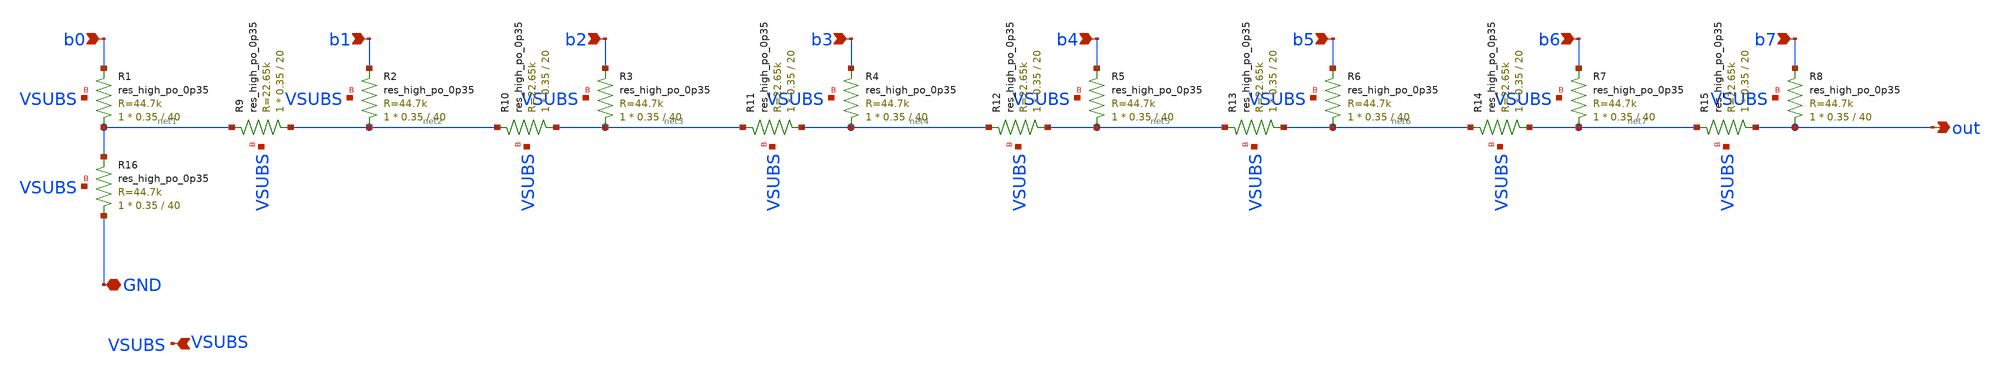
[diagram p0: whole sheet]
** sch_path: xschem/r2r.sch
**.subckt r2r b0 b1 b2 b3 b4 b5 b6 b7 out VSUBS GND
*.ipin b0
*.ipin b1
*.ipin b2
*.ipin b3
*.ipin b4
*.ipin b5
*.ipin b6
*.ipin b7
*.opin out
*.ipin VSUBS
*.iopin GND
XR1 net1 b0 VSUBS sky130_fd_pr__res_high_po_0p35 L=40 mult=1 m=1
XR2 net2 b1 VSUBS sky130_fd_pr__res_high_po_0p35 L=40 mult=1 m=1
XR3 net3 b2 VSUBS sky130_fd_pr__res_high_po_0p35 L=40 mult=1 m=1
XR4 net4 b3 VSUBS sky130_fd_pr__res_high_po_0p35 L=40 mult=1 m=1
XR5 net5 b4 VSUBS sky130_fd_pr__res_high_po_0p35 L=40 mult=1 m=1
XR6 net6 b5 VSUBS sky130_fd_pr__res_high_po_0p35 L=40 mult=1 m=1
XR7 net7 b6 VSUBS sky130_fd_pr__res_high_po_0p35 L=40 mult=1 m=1
XR8 out b7 VSUBS sky130_fd_pr__res_high_po_0p35 L=40 mult=1 m=1
XR9 net2 net1 VSUBS sky130_fd_pr__res_high_po_0p35 L=20 mult=1 m=1
XR10 net3 net2 VSUBS sky130_fd_pr__res_high_po_0p35 L=20 mult=1 m=1
XR11 net4 net3 VSUBS sky130_fd_pr__res_high_po_0p35 L=20 mult=1 m=1
XR12 net5 net4 VSUBS sky130_fd_pr__res_high_po_0p35 L=20 mult=1 m=1
XR13 net6 net5 VSUBS sky130_fd_pr__res_high_po_0p35 L=20 mult=1 m=1
XR14 net7 net6 VSUBS sky130_fd_pr__res_high_po_0p35 L=20 mult=1 m=1
XR15 out net7 VSUBS sky130_fd_pr__res_high_po_0p35 L=20 mult=1 m=1
XR16 GND net1 VSUBS sky130_fd_pr__res_high_po_0p35 L=40 mult=1 m=1
**.ends
.end
